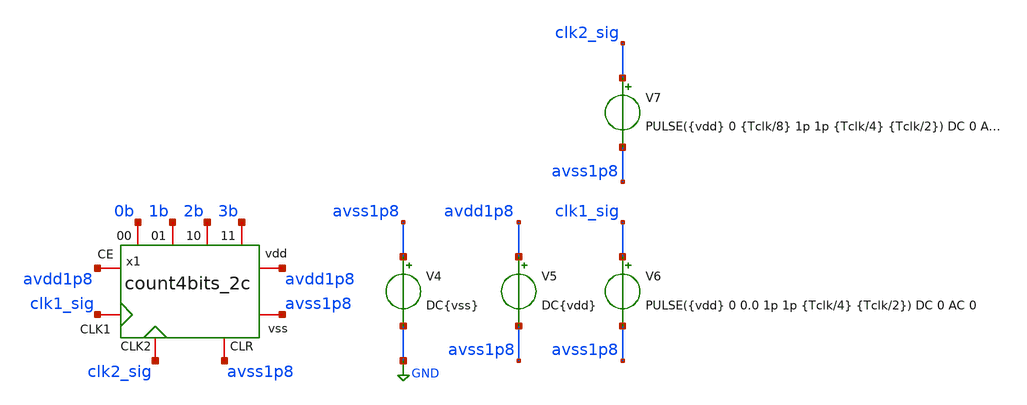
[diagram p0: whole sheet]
** sch_path: verification/testbenches/count4bits_2c/tb_count4bits_2c.sch
**.subckt tb_count4bits_2c
V4 avss1p8 GND DC{vss}
V5 avdd1p8 avss1p8 DC{vdd}
V6 clk1_sig avss1p8 PULSE({vdd} 0 0.0 1p 1p {Tclk/4} {Tclk/2}) DC 0 AC 0
x1 avdd1p8 avss1p8 avdd1p8 0b clk1_sig avss1p8 clk2_sig 1b 2b 3b count4bits_2c
V7 clk2_sig avss1p8 PULSE({vdd} 0 {Tclk/8} 1p 1p {Tclk/4} {Tclk/2}) DC 0 AC 0
**** begin user architecture code


* Circuit Parameters
.param vdd = 1.8
.param vss = 0.0
.param Tclk = 10n
.options TEMP = 65.0
* Include Models
.lib /foss/pdks/sky130A/libs.tech/ngspice/sky130.lib.spice TT
* OP Parameters & Singals to save
.save all
*Simulations
.control
tran 0.01u 100n
setplot tran1
plot v(clk1_sig)-2 v(clk2_sig) v(0b)+2 v(1b)+4 v(2b)+6 v(3b)+8
reset
dc1 V6 0 1.8 0.01
dc2 V7 0 1.8 0.01
setplot dc1
setplot dc2
set filetype = ascii
write dcsweep.raw
.endc
.end


**** end user architecture code
**.ends
.GLOBAL GND
.end
